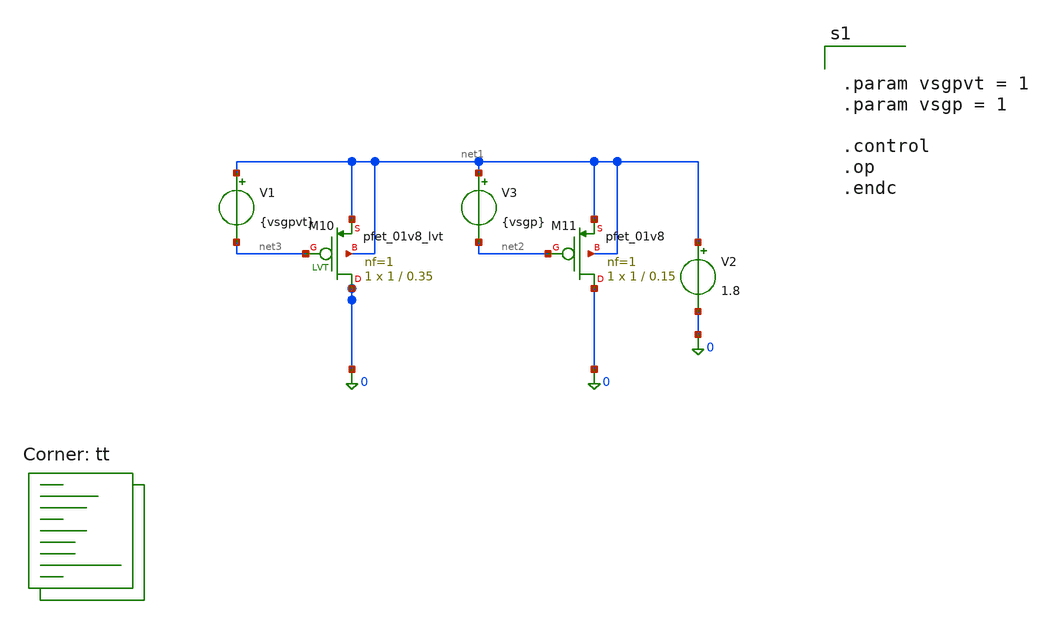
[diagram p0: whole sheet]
** sch_path: untitled.sch
**.subckt untitled
V1 net1 net3 {vsgpvt}
V2 net1 0 1.8
XM10 0 net3 net1 net1 sky130_fd_pr__pfet_01v8_lvt L=0.35 W=1 nf=1 ad='int((1 + 1)/2) * 1 / 1 * 0.29'
+ as='int((1 + 2)/2) * 1 / 1 * 0.29' pd='2*int((1 + 1)/2) * (1 / 1 + 0.29)' ps='2*int((1 + 2)/2) * (1 / 1 + 0.29)'
+ nrd='0.29 / 1 ' nrs='0.29 / 1 ' sa=0 sb=0 sd=0 mult=1 m=1
XM11 0 net2 net1 net1 sky130_fd_pr__pfet_01v8 L=0.15 W=1 nf=1 ad='int((nf+1)/2) * W/nf * 0.29' as='int((nf+2)/2) * W/nf * 0.29'
+ pd='2*int((nf+1)/2) * (W/nf + 0.29)' ps='2*int((nf+2)/2) * (W/nf + 0.29)' nrd='0.29 / W' nrs='0.29 / W'
+ sa=0 sb=0 sd=0 mult=1 m=1
V3 net1 net2 {vsgp}
**** begin user architecture code

** opencircuitdesign pdks install
.lib $::SKYWATER_MODELS/sky130.lib.spice tt



.param vsgpvt = 1
.param vsgp = 1

.control
.op
.endc



.lib $::SKYWATER_MODELS/sky130.lib.spice tt
**** end user architecture code
**.ends
.end
